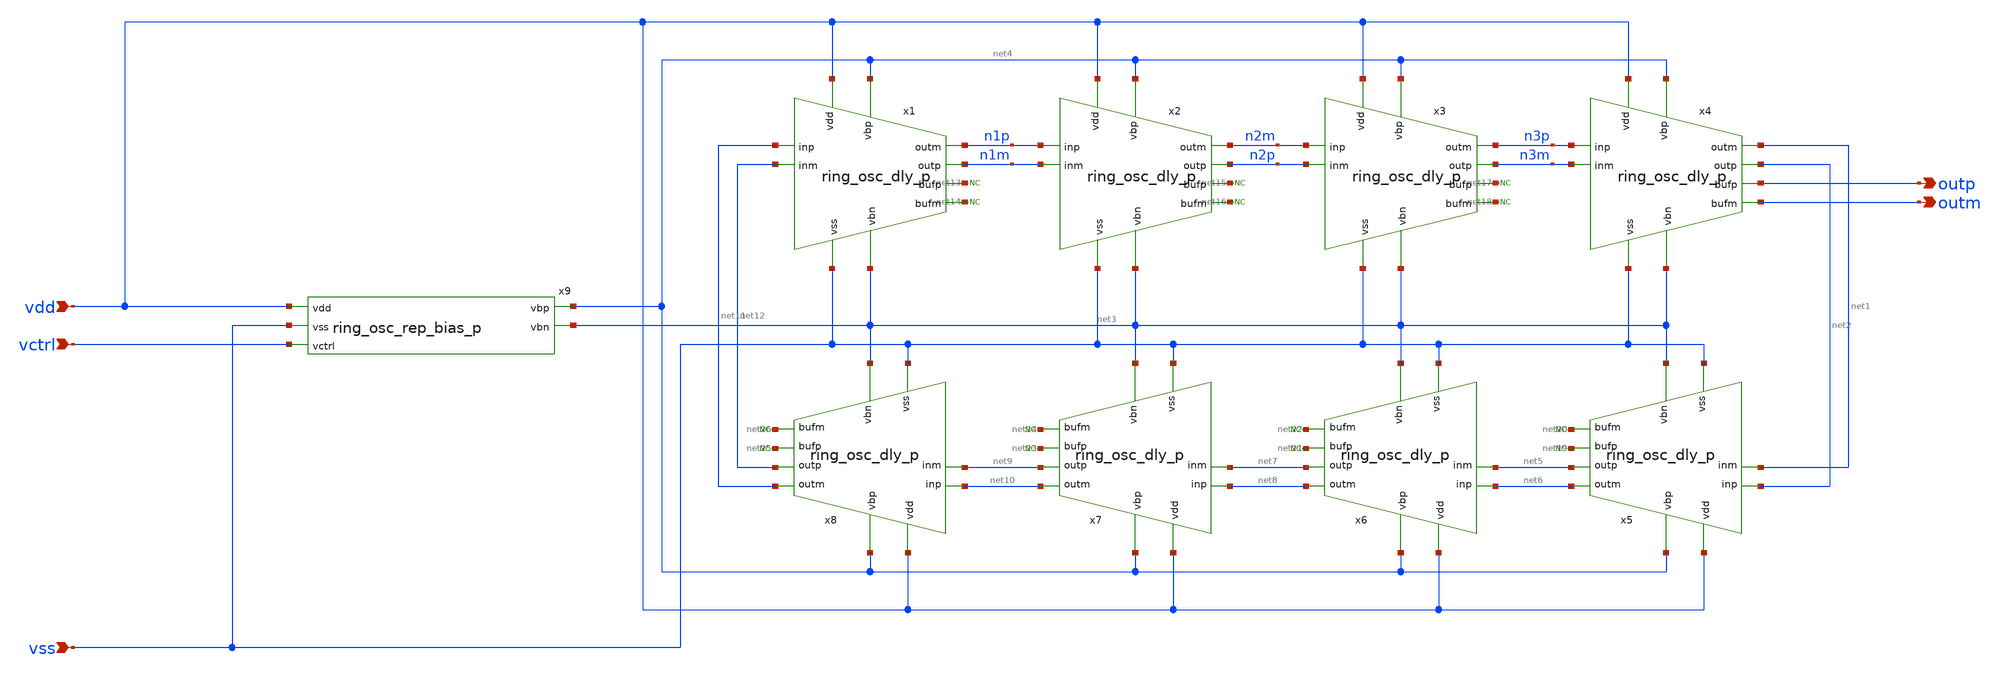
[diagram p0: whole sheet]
** sch_path: xschem/ring_osc.sch
**.subckt ring_osc vdd vss vctrl outp outm
*.ipin vdd
*.ipin vss
*.ipin vctrl
*.opin outp
*.opin outm
x1 vdd net4 net12 net11 n1p n1m net3 vss net13 net14 ring_osc_dly_p
x2 vdd net4 n1m n1p n2m n2p net3 vss net15 net16 ring_osc_dly_p
x3 vdd net4 n2p n2m n3p n3m net3 vss net17 net18 ring_osc_dly_p
x4 vdd net4 n3m n3p net1 net2 net3 vss outp outm ring_osc_dly_p
x5 vdd net4 net1 net2 net6 net5 net3 vss net19 net20 ring_osc_dly_p
x6 vdd net4 net5 net6 net8 net7 net3 vss net21 net22 ring_osc_dly_p
x7 vdd net4 net7 net8 net10 net9 net3 vss net23 net24 ring_osc_dly_p
x8 vdd net4 net9 net10 net11 net12 net3 vss net25 net26 ring_osc_dly_p
x9 vdd net4 net3 vss vctrl ring_osc_rep_bias_p
* noconn #net13
* noconn #net14
* noconn #net15
* noconn #net16
* noconn #net17
* noconn #net18
* noconn #net20
* noconn #net19
* noconn #net22
* noconn #net21
* noconn #net24
* noconn #net23
* noconn #net26
* noconn #net25
**.ends
.end
